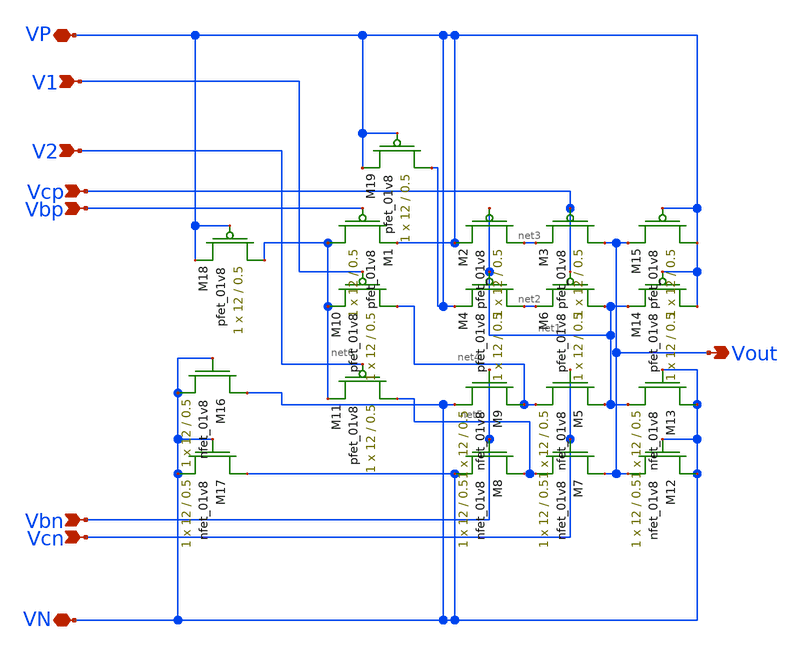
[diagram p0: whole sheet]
** sch_path: MiniProject3-Cascode/XSCHEM/Schematics/fcascodediffamp_layout.sch
**.subckt fcascodediffamp_layout VP VN V1 V2 Vbp Vcp Vcn Vbn Vout
*.iopin VP
*.iopin VN
*.ipin V1
*.ipin V2
*.ipin Vbp
*.ipin Vcp
*.ipin Vcn
*.ipin Vbn
*.opin Vout
XM5 net1 Vcn net4 VN sky130_fd_pr__nfet_01v8 L=0.5 W=12 nf=1 ad='int((nf+1)/2) * W/nf * 0.29' as='int((nf+2)/2) * W/nf * 0.29'
+ pd='2*int((nf+1)/2) * (W/nf + 0.29)' ps='2*int((nf+2)/2) * (W/nf + 0.29)' nrd='0.29 / W' nrs='0.29 / W'
+ sa=0 sb=0 sd=0 mult=1 m=1
XM2 net3 net1 VP VP sky130_fd_pr__pfet_01v8 L=0.5 W=12 nf=1 ad='int((nf+1)/2) * W/nf * 0.29' as='int((nf+2)/2) * W/nf * 0.29'
+ pd='2*int((nf+1)/2) * (W/nf + 0.29)' ps='2*int((nf+2)/2) * (W/nf + 0.29)' nrd='0.29 / W' nrs='0.29 / W'
+ sa=0 sb=0 sd=0 mult=1 m=1
XM3 Vout Vcp net3 VP sky130_fd_pr__pfet_01v8 L=0.5 W=12 nf=1 ad='int((nf+1)/2) * W/nf * 0.29' as='int((nf+2)/2) * W/nf * 0.29'
+ pd='2*int((nf+1)/2) * (W/nf + 0.29)' ps='2*int((nf+2)/2) * (W/nf + 0.29)' nrd='0.29 / W' nrs='0.29 / W'
+ sa=0 sb=0 sd=0 mult=1 m=1
XM4 net2 net1 VP VP sky130_fd_pr__pfet_01v8 L=0.5 W=12 nf=1 ad='int((nf+1)/2) * W/nf * 0.29' as='int((nf+2)/2) * W/nf * 0.29'
+ pd='2*int((nf+1)/2) * (W/nf + 0.29)' ps='2*int((nf+2)/2) * (W/nf + 0.29)' nrd='0.29 / W' nrs='0.29 / W'
+ sa=0 sb=0 sd=0 mult=1 m=1
XM6 net1 Vcp net2 VP sky130_fd_pr__pfet_01v8 L=0.5 W=12 nf=1 ad='int((nf+1)/2) * W/nf * 0.29' as='int((nf+2)/2) * W/nf * 0.29'
+ pd='2*int((nf+1)/2) * (W/nf + 0.29)' ps='2*int((nf+2)/2) * (W/nf + 0.29)' nrd='0.29 / W' nrs='0.29 / W'
+ sa=0 sb=0 sd=0 mult=1 m=1
XM7 Vout Vcn net5 VN sky130_fd_pr__nfet_01v8 L=0.5 W=12 nf=1 ad='int((nf+1)/2) * W/nf * 0.29' as='int((nf+2)/2) * W/nf * 0.29'
+ pd='2*int((nf+1)/2) * (W/nf + 0.29)' ps='2*int((nf+2)/2) * (W/nf + 0.29)' nrd='0.29 / W' nrs='0.29 / W'
+ sa=0 sb=0 sd=0 mult=1 m=1
XM8 net5 Vbn VN VN sky130_fd_pr__nfet_01v8 L=0.5 W=12 nf=1 ad='int((nf+1)/2) * W/nf * 0.29' as='int((nf+2)/2) * W/nf * 0.29'
+ pd='2*int((nf+1)/2) * (W/nf + 0.29)' ps='2*int((nf+2)/2) * (W/nf + 0.29)' nrd='0.29 / W' nrs='0.29 / W'
+ sa=0 sb=0 sd=0 mult=1 m=1
XM9 net4 Vbn VN VN sky130_fd_pr__nfet_01v8 L=0.5 W=12 nf=1 ad='int((nf+1)/2) * W/nf * 0.29' as='int((nf+2)/2) * W/nf * 0.29'
+ pd='2*int((nf+1)/2) * (W/nf + 0.29)' ps='2*int((nf+2)/2) * (W/nf + 0.29)' nrd='0.29 / W' nrs='0.29 / W'
+ sa=0 sb=0 sd=0 mult=1 m=1
XM12 VN VN Vout VN sky130_fd_pr__nfet_01v8 L=0.5 W=12 nf=1 ad='int((nf+1)/2) * W/nf * 0.29' as='int((nf+2)/2) * W/nf * 0.29'
+ pd='2*int((nf+1)/2) * (W/nf + 0.29)' ps='2*int((nf+2)/2) * (W/nf + 0.29)' nrd='0.29 / W' nrs='0.29 / W'
+ sa=0 sb=0 sd=0 mult=1 m=1
XM13 VN VN net1 VN sky130_fd_pr__nfet_01v8 L=0.5 W=12 nf=1 ad='int((nf+1)/2) * W/nf * 0.29' as='int((nf+2)/2) * W/nf * 0.29'
+ pd='2*int((nf+1)/2) * (W/nf + 0.29)' ps='2*int((nf+2)/2) * (W/nf + 0.29)' nrd='0.29 / W' nrs='0.29 / W'
+ sa=0 sb=0 sd=0 mult=1 m=1
XM14 VP VP net1 VP sky130_fd_pr__pfet_01v8 L=0.5 W=12 nf=1 ad='int((nf+1)/2) * W/nf * 0.29' as='int((nf+2)/2) * W/nf * 0.29'
+ pd='2*int((nf+1)/2) * (W/nf + 0.29)' ps='2*int((nf+2)/2) * (W/nf + 0.29)' nrd='0.29 / W' nrs='0.29 / W'
+ sa=0 sb=0 sd=0 mult=1 m=1
XM15 VP VP Vout VP sky130_fd_pr__pfet_01v8 L=0.5 W=12 nf=1 ad='int((nf+1)/2) * W/nf * 0.29' as='int((nf+2)/2) * W/nf * 0.29'
+ pd='2*int((nf+1)/2) * (W/nf + 0.29)' ps='2*int((nf+2)/2) * (W/nf + 0.29)' nrd='0.29 / W' nrs='0.29 / W'
+ sa=0 sb=0 sd=0 mult=1 m=1
XM1 net6 Vbp VP VP sky130_fd_pr__pfet_01v8 L=0.5 W=12 nf=1 ad='int((nf+1)/2) * W/nf * 0.29' as='int((nf+2)/2) * W/nf * 0.29'
+ pd='2*int((nf+1)/2) * (W/nf + 0.29)' ps='2*int((nf+2)/2) * (W/nf + 0.29)' nrd='0.29 / W' nrs='0.29 / W'
+ sa=0 sb=0 sd=0 mult=1 m=1
XM10 net4 V1 net6 VP sky130_fd_pr__pfet_01v8 L=0.5 W=12 nf=1 ad='int((nf+1)/2) * W/nf * 0.29' as='int((nf+2)/2) * W/nf * 0.29'
+ pd='2*int((nf+1)/2) * (W/nf + 0.29)' ps='2*int((nf+2)/2) * (W/nf + 0.29)' nrd='0.29 / W' nrs='0.29 / W'
+ sa=0 sb=0 sd=0 mult=1 m=1
XM11 net5 V2 net6 VP sky130_fd_pr__pfet_01v8 L=0.5 W=12 nf=1 ad='int((nf+1)/2) * W/nf * 0.29' as='int((nf+2)/2) * W/nf * 0.29'
+ pd='2*int((nf+1)/2) * (W/nf + 0.29)' ps='2*int((nf+2)/2) * (W/nf + 0.29)' nrd='0.29 / W' nrs='0.29 / W'
+ sa=0 sb=0 sd=0 mult=1 m=1
XM16 VN VN VN VN sky130_fd_pr__nfet_01v8 L=0.5 W=12 nf=1 ad='int((nf+1)/2) * W/nf * 0.29' as='int((nf+2)/2) * W/nf * 0.29'
+ pd='2*int((nf+1)/2) * (W/nf + 0.29)' ps='2*int((nf+2)/2) * (W/nf + 0.29)' nrd='0.29 / W' nrs='0.29 / W'
+ sa=0 sb=0 sd=0 mult=1 m=1
XM17 VN VN VN VN sky130_fd_pr__nfet_01v8 L=0.5 W=12 nf=1 ad='int((nf+1)/2) * W/nf * 0.29' as='int((nf+2)/2) * W/nf * 0.29'
+ pd='2*int((nf+1)/2) * (W/nf + 0.29)' ps='2*int((nf+2)/2) * (W/nf + 0.29)' nrd='0.29 / W' nrs='0.29 / W'
+ sa=0 sb=0 sd=0 mult=1 m=1
XM18 net6 VP VP VP sky130_fd_pr__pfet_01v8 L=0.5 W=12 nf=1 ad='int((nf+1)/2) * W/nf * 0.29' as='int((nf+2)/2) * W/nf * 0.29'
+ pd='2*int((nf+1)/2) * (W/nf + 0.29)' ps='2*int((nf+2)/2) * (W/nf + 0.29)' nrd='0.29 / W' nrs='0.29 / W'
+ sa=0 sb=0 sd=0 mult=1 m=1
XM19 VP VP VP VP sky130_fd_pr__pfet_01v8 L=0.5 W=12 nf=1 ad='int((nf+1)/2) * W/nf * 0.29' as='int((nf+2)/2) * W/nf * 0.29'
+ pd='2*int((nf+1)/2) * (W/nf + 0.29)' ps='2*int((nf+2)/2) * (W/nf + 0.29)' nrd='0.29 / W' nrs='0.29 / W'
+ sa=0 sb=0 sd=0 mult=1 m=1
**.ends
.end
